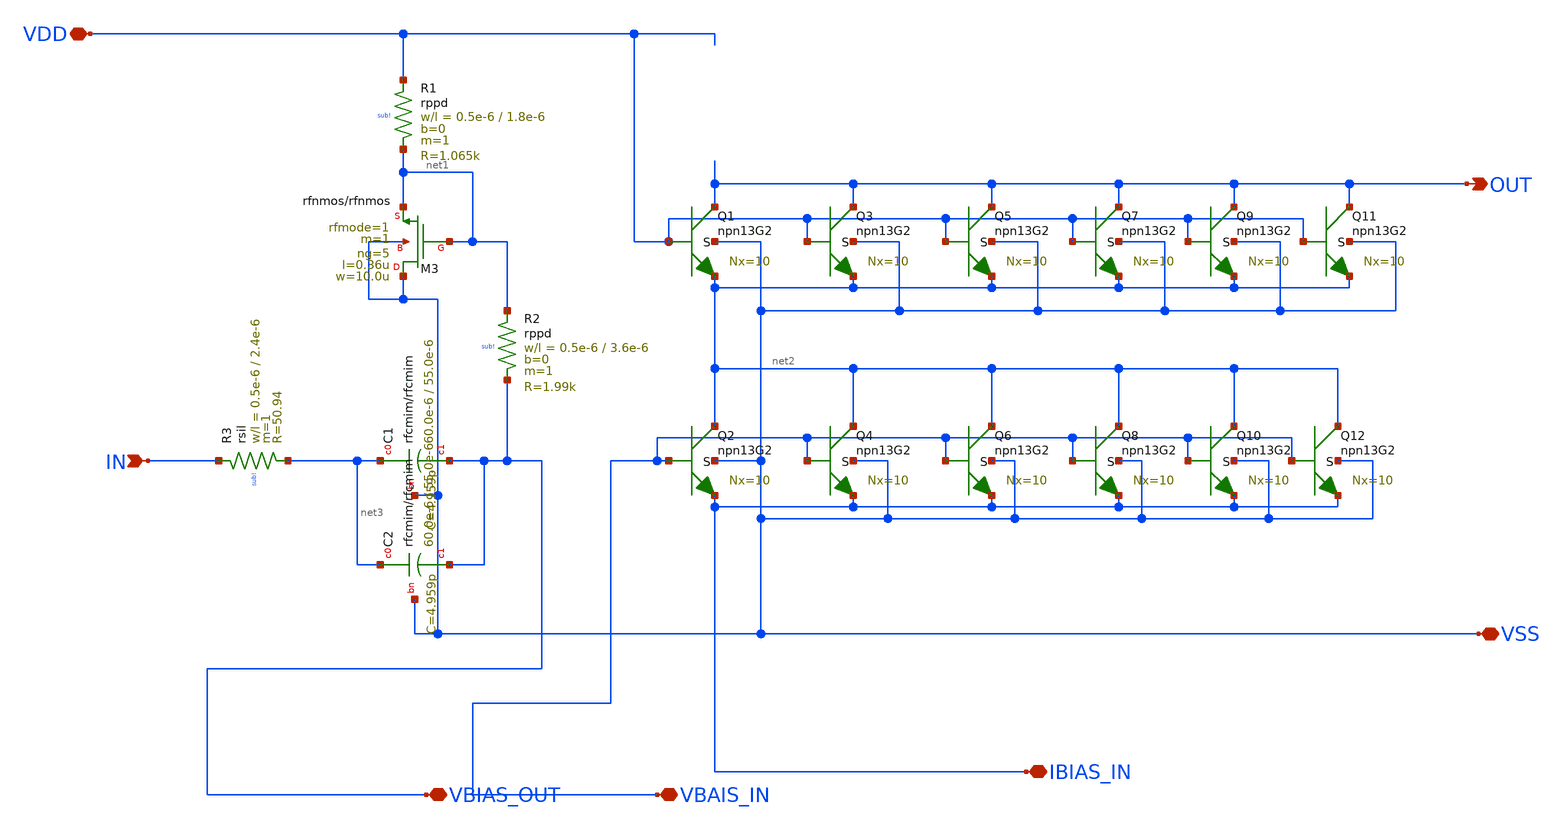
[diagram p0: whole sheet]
** sch_path: GPS_LNA/design_data/xschem/lna_npn_base.sch
**.subckt lna_npn_base VDD IN OUT VSS VBAIS_IN VBIAS_OUT IBIAS_IN
*.iopin VDD
*.ipin IN
*.opin OUT
*.iopin VSS
*.iopin VBAIS_IN
*.iopin VBIAS_OUT
*.iopin IBIAS_IN
XR2 net1 VBIAS_OUT sub! rppd w=0.5e-6 l=3.6e-6 m=1 b=0 mm_ok=1
XR1 VDD net1 sub! rppd w=0.5e-6 l=1.8e-6 m=1 b=0 mm_ok=1
XR3 IN net3 sub! rsil w=0.5e-6 l=2.4e-6 m=1 mm_ok=1
XC1 net3 VBIAS_OUT VSS rfcmim w=60.0e-6 l=55.0e-6 wfeed=5.0e-6 m=1 mm_ok=1
XC2 net3 VBIAS_OUT VSS rfcmim w=60.0e-6 l=55.0e-6 wfeed=5.0e-6 m=1 mm_ok=1
XM3 VSS net1 net1 VSS rfnmos w=10.0u l=0.36u ng=5 m=1 rfmode=1 mm_ok=1
XQ1 OUT VDD net2 VSS npn13G2 Nx=10 mm_ok=1
XQ2 net2 VBAIS_IN IBIAS_IN VSS npn13G2 Nx=10 mm_ok=1
XQ3 OUT VDD net2 VSS npn13G2 Nx=10 mm_ok=1
XQ4 net2 VBAIS_IN IBIAS_IN VSS npn13G2 Nx=10 mm_ok=1
XQ5 OUT VDD net2 VSS npn13G2 Nx=10 mm_ok=1
XQ6 net2 VBAIS_IN IBIAS_IN VSS npn13G2 Nx=10 mm_ok=1
XQ7 OUT VDD net2 VSS npn13G2 Nx=10 mm_ok=1
XQ8 net2 VBAIS_IN IBIAS_IN VSS npn13G2 Nx=10 mm_ok=1
XQ9 OUT VDD net2 VSS npn13G2 Nx=10 mm_ok=1
XQ10 net2 VBAIS_IN IBIAS_IN VSS npn13G2 Nx=10 mm_ok=1
XQ11 OUT VDD net2 VSS npn13G2 Nx=10 mm_ok=1
XQ12 net2 VBAIS_IN IBIAS_IN VSS npn13G2 Nx=10 mm_ok=1
**.ends
.end
